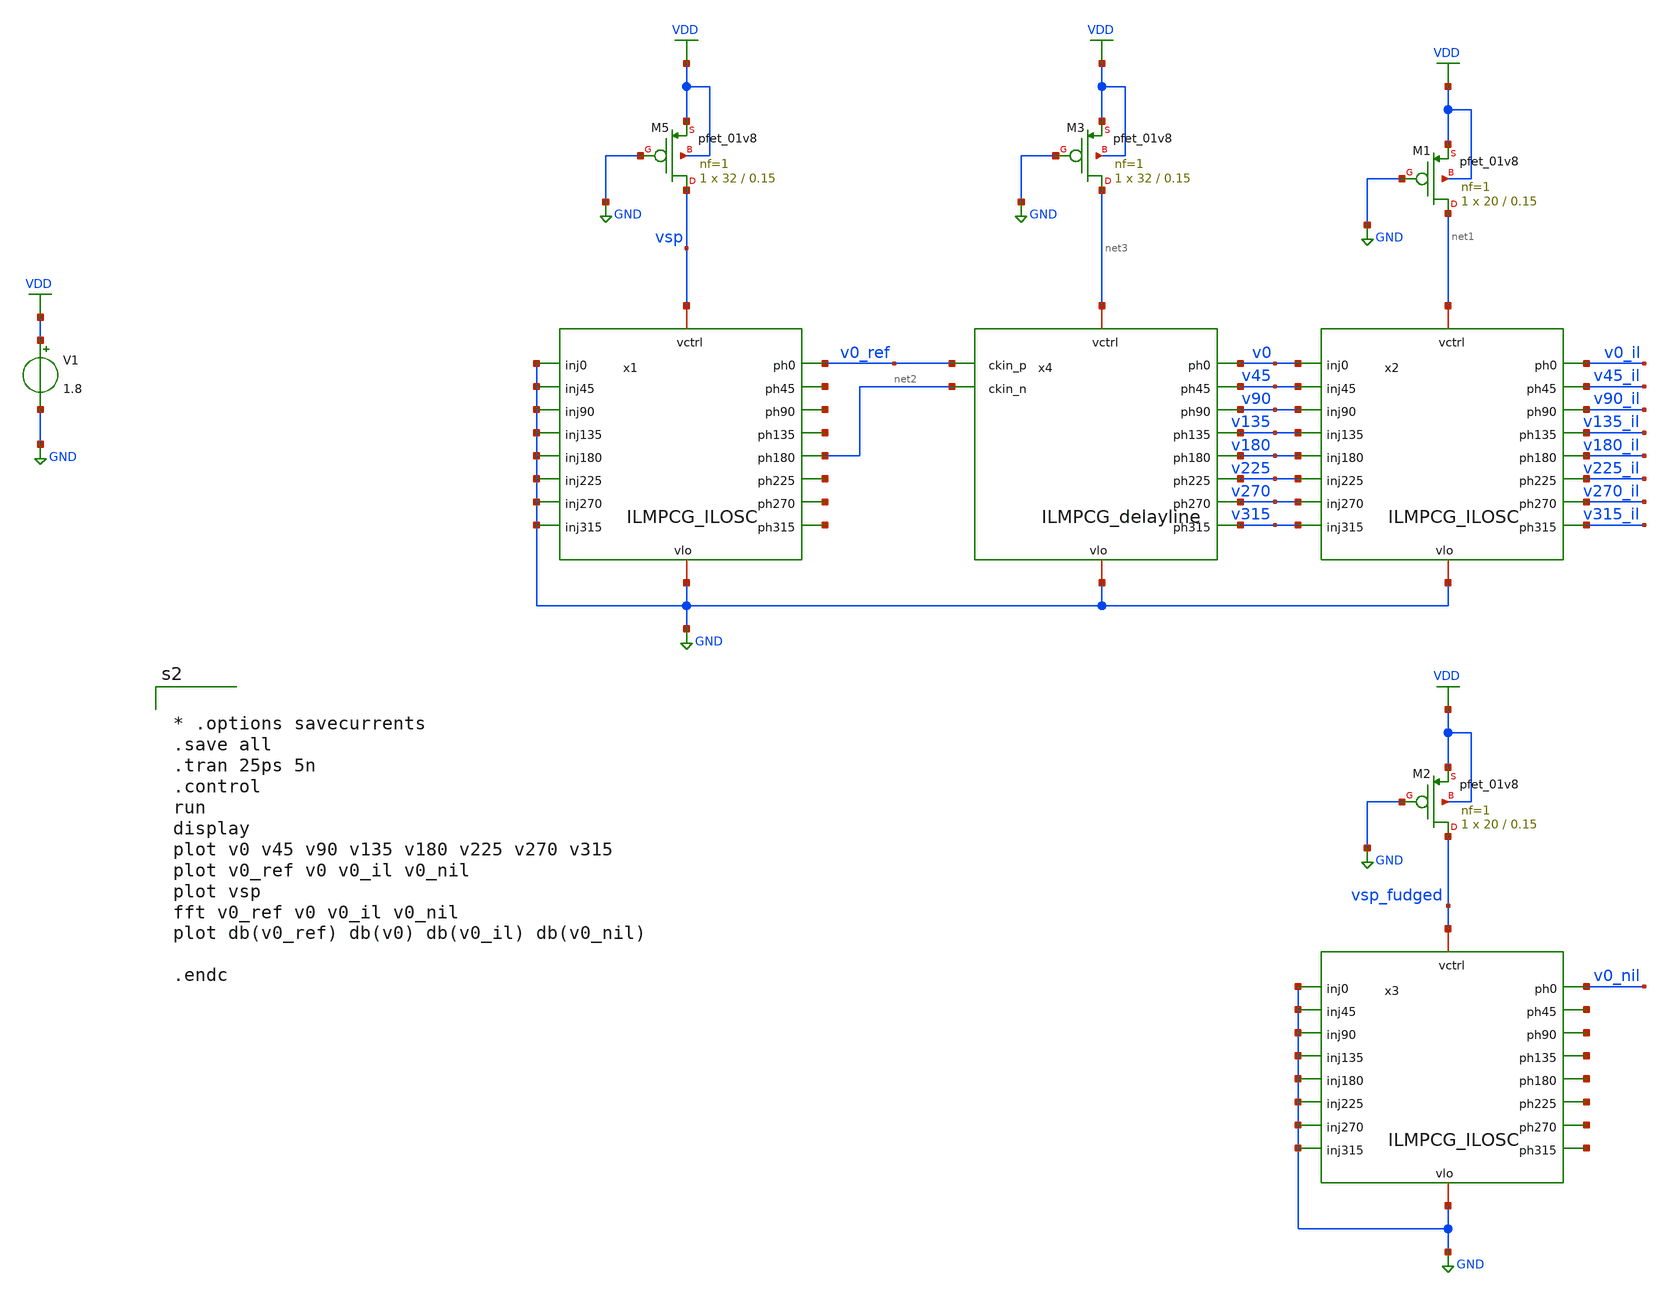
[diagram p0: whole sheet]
** sch_path: xschem/xcp_osc_tb.sch
**.subckt xcp_osc_tb
V1 VDD GND 1.8
XM5 vsp GND VDD VDD sky130_fd_pr__pfet_01v8 L=0.15 W=32 nf=1 ad='int((nf+1)/2) * W/nf * 0.29' as='int((nf+2)/2) * W/nf * 0.29'
+ pd='2*int((nf+1)/2) * (W/nf + 0.29)' ps='2*int((nf+2)/2) * (W/nf + 0.29)' nrd='0.29 / W' nrs='0.29 / W'
+ sa=0 sb=0 sd=0 mult=1 m=1
x1 vsp v0_ref net4 net5 net6 net2 net7 net8 net9 GND GND GND GND GND GND GND GND GND ILMPCG_ILOSC
x2 net1 v0_il v45_il v90_il v135_il v180_il v225_il v270_il v315_il v0 v45 v90 v135 v180 v225 v270
+ v315 GND ILMPCG_ILOSC
XM1 net1 GND VDD VDD sky130_fd_pr__pfet_01v8 L=0.15 W=20 nf=1 ad='int((nf+1)/2) * W/nf * 0.29' as='int((nf+2)/2) * W/nf * 0.29'
+ pd='2*int((nf+1)/2) * (W/nf + 0.29)' ps='2*int((nf+2)/2) * (W/nf + 0.29)' nrd='0.29 / W' nrs='0.29 / W'
+ sa=0 sb=0 sd=0 mult=1 m=1
x3 vsp_fudged v0_nil net10 net11 net12 net13 net14 net15 net16 GND GND GND GND GND GND GND GND GND
+ ILMPCG_ILOSC
XM2 vsp_fudged GND VDD VDD sky130_fd_pr__pfet_01v8 L=0.15 W=20 nf=1 ad='int((nf+1)/2) * W/nf * 0.29'
+ as='int((nf+2)/2) * W/nf * 0.29' pd='2*int((nf+1)/2) * (W/nf + 0.29)' ps='2*int((nf+2)/2) * (W/nf + 0.29)'
+ nrd='0.29 / W' nrs='0.29 / W' sa=0 sb=0 sd=0 mult=1 m=1
x4 net3 v0 v45 v90 v135 v180 v225 v270 v315 GND v0_ref net2 ILMPCG_delayline
XM3 net3 GND VDD VDD sky130_fd_pr__pfet_01v8 L=0.15 W=32 nf=1 ad='int((nf+1)/2) * W/nf * 0.29' as='int((nf+2)/2) * W/nf * 0.29'
+ pd='2*int((nf+1)/2) * (W/nf + 0.29)' ps='2*int((nf+2)/2) * (W/nf + 0.29)' nrd='0.29 / W' nrs='0.29 / W'
+ sa=0 sb=0 sd=0 mult=1 m=1
**** begin user architecture code
.lib $::SKYWATER_MODELS/sky130.lib.spice tt
* .include $::PDKPATH/libs.ref/sky130_fd_sc_hvl/spice/sky130_fd_sc_hvl.spice



* .options savecurrents
.save all
.tran 25ps 5n
.control
run
display
plot v0 v45 v90 v135 v180 v225 v270 v315
plot v0_ref v0 v0_il v0_nil
plot vsp
fft v0_ref v0 v0_il v0_nil
plot db(v0_ref) db(v0) db(v0_il) db(v0_nil)

.endc


**** end user architecture code
**.ends
.GLOBAL VDD
.GLOBAL GND
.end
